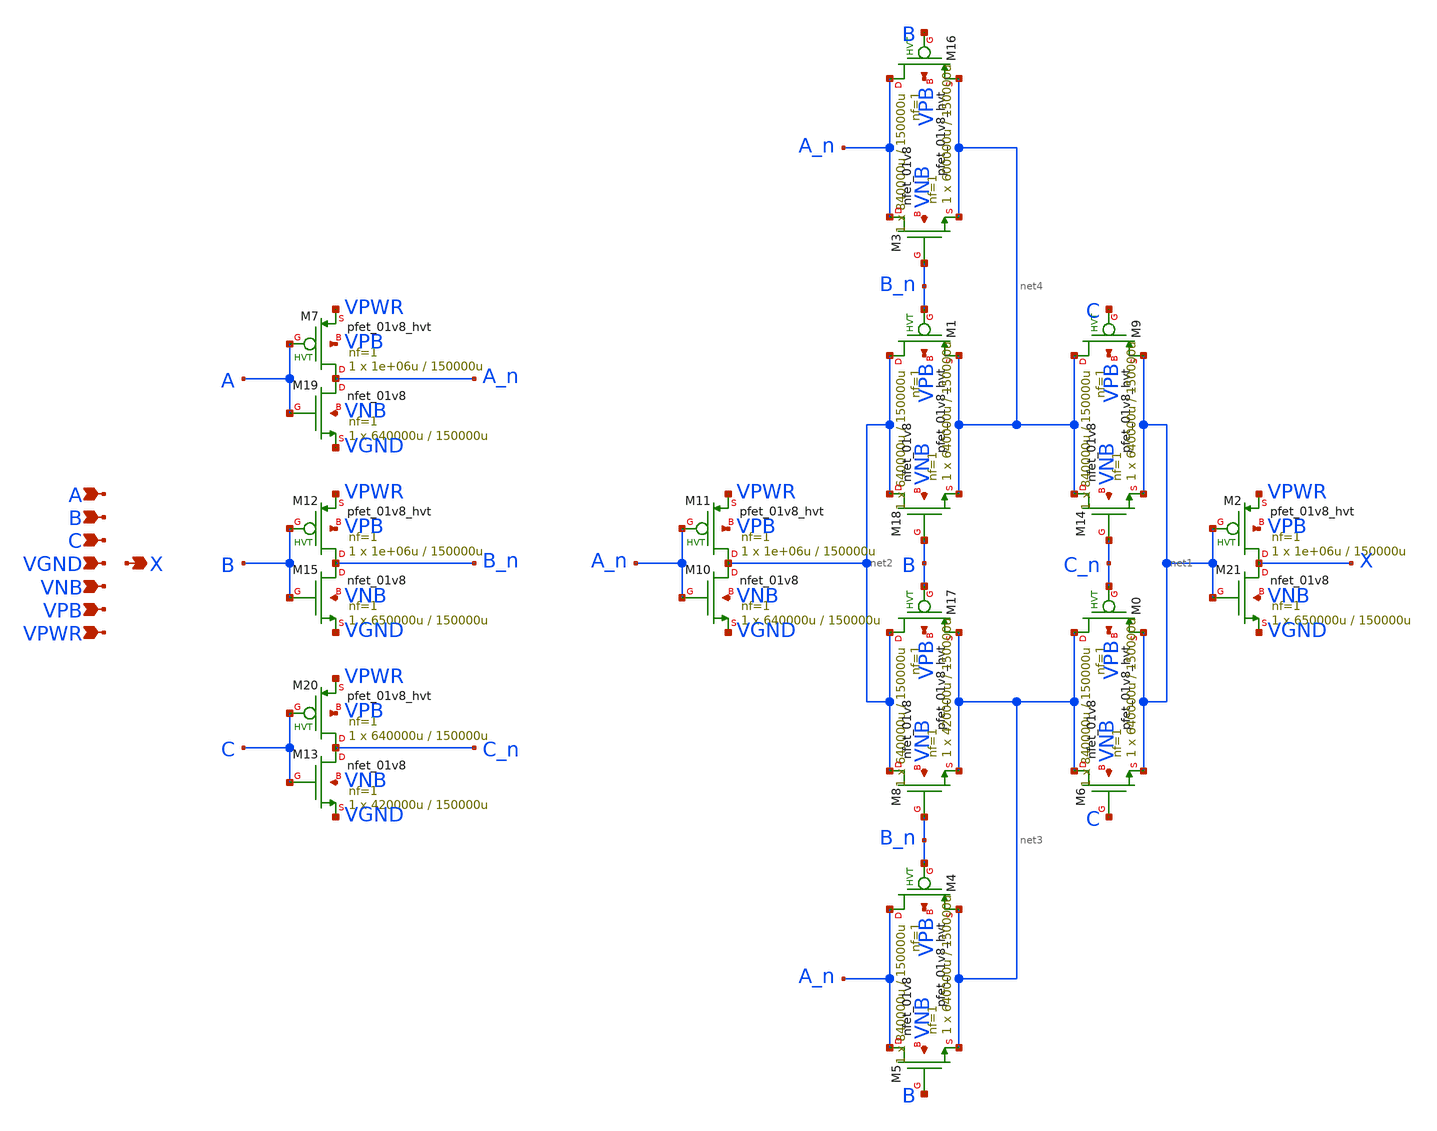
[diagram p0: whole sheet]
** sch_path: schematics/xor3/sky130_fd_sc_hd__xor3_1.sch
**.subckt sky130_fd_sc_hd__xor3_1 A B C VGND VNB VPB VPWR X
*.ipin A
*.ipin B
*.ipin C
*.ipin VGND
*.ipin VNB
*.ipin VPB
*.ipin VPWR
*.opin X
XM7 A_n A VPWR VPB sky130_fd_pr__pfet_01v8_hvt L=150000u W=1e+06u nf=1 ad='int((1 + 1)/2) * 1e+06u / 1 * 0.29'
+ as='int((1 + 2)/2) * 1e+06u / 1 * 0.29' pd='2*int((1 + 1)/2) * (1e+06u / 1 + 0.29)' ps='2*int((1 + 2)/2) * (1e+06u / 1 + 0.29)'
+ nrd='0.29 / 1e+06u ' nrs='0.29 / 1e+06u ' sa=0 sb=0 sd=0 mult=1 m=1
XM19 A_n A VGND VNB sky130_fd_pr__nfet_01v8 L=150000u W=640000u nf=1 ad='int((1 + 1)/2) * 640000u / 1 * 0.29'
+ as='int((1 + 2)/2) * 640000u / 1 * 0.29' pd='2*int((1 + 1)/2) * (640000u / 1 + 0.29)' ps='2*int((1 + 2)/2) * (640000u / 1 + 0.29)'
+ nrd='0.29 / 640000u ' nrs='0.29 / 640000u ' sa=0 sb=0 sd=0 mult=1 m=1
XM2 X net1 VPWR VPB sky130_fd_pr__pfet_01v8_hvt L=150000u W=1e+06u nf=1 ad='int((1 + 1)/2) * 1e+06u / 1 * 0.29'
+ as='int((1 + 2)/2) * 1e+06u / 1 * 0.29' pd='2*int((1 + 1)/2) * (1e+06u / 1 + 0.29)' ps='2*int((1 + 2)/2) * (1e+06u / 1 + 0.29)'
+ nrd='0.29 / 1e+06u ' nrs='0.29 / 1e+06u ' sa=0 sb=0 sd=0 mult=1 m=1
XM21 X net1 VGND VNB sky130_fd_pr__nfet_01v8 L=150000u W=650000u nf=1 ad='int((1 + 1)/2) * 650000u / 1 * 0.29'
+ as='int((1 + 2)/2) * 650000u / 1 * 0.29' pd='2*int((1 + 1)/2) * (650000u / 1 + 0.29)' ps='2*int((1 + 2)/2) * (650000u / 1 + 0.29)'
+ nrd='0.29 / 650000u ' nrs='0.29 / 650000u ' sa=0 sb=0 sd=0 mult=1 m=1
XM11 net2 A_n VPWR VPB sky130_fd_pr__pfet_01v8_hvt L=150000u W=1e+06u nf=1 ad='int((1 + 1)/2) * 1e+06u / 1 * 0.29'
+ as='int((1 + 2)/2) * 1e+06u / 1 * 0.29' pd='2*int((1 + 1)/2) * (1e+06u / 1 + 0.29)' ps='2*int((1 + 2)/2) * (1e+06u / 1 + 0.29)'
+ nrd='0.29 / 1e+06u ' nrs='0.29 / 1e+06u ' sa=0 sb=0 sd=0 mult=1 m=1
XM10 net2 A_n VGND VNB sky130_fd_pr__nfet_01v8 L=150000u W=640000u nf=1 ad='int((1 + 1)/2) * 640000u / 1 * 0.29'
+ as='int((1 + 2)/2) * 640000u / 1 * 0.29' pd='2*int((1 + 1)/2) * (640000u / 1 + 0.29)' ps='2*int((1 + 2)/2) * (640000u / 1 + 0.29)'
+ nrd='0.29 / 640000u ' nrs='0.29 / 640000u ' sa=0 sb=0 sd=0 mult=1 m=1
XM12 B_n B VPWR VPB sky130_fd_pr__pfet_01v8_hvt L=150000u W=1e+06u nf=1 ad='int((1 + 1)/2) * 1e+06u / 1 * 0.29'
+ as='int((1 + 2)/2) * 1e+06u / 1 * 0.29' pd='2*int((1 + 1)/2) * (1e+06u / 1 + 0.29)' ps='2*int((1 + 2)/2) * (1e+06u / 1 + 0.29)'
+ nrd='0.29 / 1e+06u ' nrs='0.29 / 1e+06u ' sa=0 sb=0 sd=0 mult=1 m=1
XM15 B_n B VGND VNB sky130_fd_pr__nfet_01v8 L=150000u W=650000u nf=1 ad='int((1 + 1)/2) * 650000u / 1 * 0.29'
+ as='int((1 + 2)/2) * 650000u / 1 * 0.29' pd='2*int((1 + 1)/2) * (650000u / 1 + 0.29)' ps='2*int((1 + 2)/2) * (650000u / 1 + 0.29)'
+ nrd='0.29 / 650000u ' nrs='0.29 / 650000u ' sa=0 sb=0 sd=0 mult=1 m=1
XM20 C_n C VPWR VPB sky130_fd_pr__pfet_01v8_hvt L=150000u W=640000u nf=1 ad='int((1 + 1)/2) * 640000u / 1 * 0.29'
+ as='int((1 + 2)/2) * 640000u / 1 * 0.29' pd='2*int((1 + 1)/2) * (640000u / 1 + 0.29)' ps='2*int((1 + 2)/2) * (640000u / 1 + 0.29)'
+ nrd='0.29 / 640000u ' nrs='0.29 / 640000u ' sa=0 sb=0 sd=0 mult=1 m=1
XM13 C_n C VGND VNB sky130_fd_pr__nfet_01v8 L=150000u W=420000u nf=1 ad='int((1 + 1)/2) * 420000u / 1 * 0.29'
+ as='int((1 + 2)/2) * 420000u / 1 * 0.29' pd='2*int((1 + 1)/2) * (420000u / 1 + 0.29)' ps='2*int((1 + 2)/2) * (420000u / 1 + 0.29)'
+ nrd='0.29 / 420000u ' nrs='0.29 / 420000u ' sa=0 sb=0 sd=0 mult=1 m=1
XM0 net3 C_n net1 VPB sky130_fd_pr__pfet_01v8_hvt L=150000u W=840000u nf=1 ad='int((1 + 1)/2) * 840000u / 1 * 0.29'
+ as='int((1 + 2)/2) * 840000u / 1 * 0.29' pd='2*int((1 + 1)/2) * (840000u / 1 + 0.29)' ps='2*int((1 + 2)/2) * (840000u / 1 + 0.29)'
+ nrd='0.29 / 840000u ' nrs='0.29 / 840000u ' sa=0 sb=0 sd=0 mult=1 m=1
XM6 net3 C net1 VNB sky130_fd_pr__nfet_01v8 L=150000u W=640000u nf=1 ad='int((1 + 1)/2) * 640000u / 1 * 0.29'
+ as='int((1 + 2)/2) * 640000u / 1 * 0.29' pd='2*int((1 + 1)/2) * (640000u / 1 + 0.29)' ps='2*int((1 + 2)/2) * (640000u / 1 + 0.29)'
+ nrd='0.29 / 640000u ' nrs='0.29 / 640000u ' sa=0 sb=0 sd=0 mult=1 m=1
XM1 net2 B_n net4 VPB sky130_fd_pr__pfet_01v8_hvt L=150000u W=640000u nf=1 ad='int((1 + 1)/2) * 640000u / 1 * 0.29'
+ as='int((1 + 2)/2) * 640000u / 1 * 0.29' pd='2*int((1 + 1)/2) * (640000u / 1 + 0.29)' ps='2*int((1 + 2)/2) * (640000u / 1 + 0.29)'
+ nrd='0.29 / 640000u ' nrs='0.29 / 640000u ' sa=0 sb=0 sd=0 mult=1 m=1
XM18 net2 B net4 VNB sky130_fd_pr__nfet_01v8 L=150000u W=640000u nf=1 ad='int((1 + 1)/2) * 640000u / 1 * 0.29'
+ as='int((1 + 2)/2) * 640000u / 1 * 0.29' pd='2*int((1 + 1)/2) * (640000u / 1 + 0.29)' ps='2*int((1 + 2)/2) * (640000u / 1 + 0.29)'
+ nrd='0.29 / 640000u ' nrs='0.29 / 640000u ' sa=0 sb=0 sd=0 mult=1 m=1
XM4 A_n B_n net3 VPB sky130_fd_pr__pfet_01v8_hvt L=150000u W=840000u nf=1 ad='int((1 + 1)/2) * 840000u / 1 * 0.29'
+ as='int((1 + 2)/2) * 840000u / 1 * 0.29' pd='2*int((1 + 1)/2) * (840000u / 1 + 0.29)' ps='2*int((1 + 2)/2) * (840000u / 1 + 0.29)'
+ nrd='0.29 / 840000u ' nrs='0.29 / 840000u ' sa=0 sb=0 sd=0 mult=1 m=1
XM5 A_n B net3 VNB sky130_fd_pr__nfet_01v8 L=150000u W=640000u nf=1 ad='int((1 + 1)/2) * 640000u / 1 * 0.29'
+ as='int((1 + 2)/2) * 640000u / 1 * 0.29' pd='2*int((1 + 1)/2) * (640000u / 1 + 0.29)' ps='2*int((1 + 2)/2) * (640000u / 1 + 0.29)'
+ nrd='0.29 / 640000u ' nrs='0.29 / 640000u ' sa=0 sb=0 sd=0 mult=1 m=1
XM16 A_n B net4 VPB sky130_fd_pr__pfet_01v8_hvt L=150000u W=840000u nf=1 ad='int((1 + 1)/2) * 840000u / 1 * 0.29'
+ as='int((1 + 2)/2) * 840000u / 1 * 0.29' pd='2*int((1 + 1)/2) * (840000u / 1 + 0.29)' ps='2*int((1 + 2)/2) * (840000u / 1 + 0.29)'
+ nrd='0.29 / 840000u ' nrs='0.29 / 840000u ' sa=0 sb=0 sd=0 mult=1 m=1
XM3 A_n B_n net4 VNB sky130_fd_pr__nfet_01v8 L=150000u W=600000u nf=1 ad='int((1 + 1)/2) * 600000u / 1 * 0.29'
+ as='int((1 + 2)/2) * 600000u / 1 * 0.29' pd='2*int((1 + 1)/2) * (600000u / 1 + 0.29)' ps='2*int((1 + 2)/2) * (600000u / 1 + 0.29)'
+ nrd='0.29 / 600000u ' nrs='0.29 / 600000u ' sa=0 sb=0 sd=0 mult=1 m=1
XM17 net2 B net3 VPB sky130_fd_pr__pfet_01v8_hvt L=150000u W=640000u nf=1 ad='int((1 + 1)/2) * 640000u / 1 * 0.29'
+ as='int((1 + 2)/2) * 640000u / 1 * 0.29' pd='2*int((1 + 1)/2) * (640000u / 1 + 0.29)' ps='2*int((1 + 2)/2) * (640000u / 1 + 0.29)'
+ nrd='0.29 / 640000u ' nrs='0.29 / 640000u ' sa=0 sb=0 sd=0 mult=1 m=1
XM8 net2 B_n net3 VNB sky130_fd_pr__nfet_01v8 L=150000u W=420000u nf=1 ad='int((1 + 1)/2) * 420000u / 1 * 0.29'
+ as='int((1 + 2)/2) * 420000u / 1 * 0.29' pd='2*int((1 + 1)/2) * (420000u / 1 + 0.29)' ps='2*int((1 + 2)/2) * (420000u / 1 + 0.29)'
+ nrd='0.29 / 420000u ' nrs='0.29 / 420000u ' sa=0 sb=0 sd=0 mult=1 m=1
XM9 net4 C net1 VPB sky130_fd_pr__pfet_01v8_hvt L=150000u W=840000u nf=1 ad='int((1 + 1)/2) * 840000u / 1 * 0.29'
+ as='int((1 + 2)/2) * 840000u / 1 * 0.29' pd='2*int((1 + 1)/2) * (840000u / 1 + 0.29)' ps='2*int((1 + 2)/2) * (840000u / 1 + 0.29)'
+ nrd='0.29 / 840000u ' nrs='0.29 / 840000u ' sa=0 sb=0 sd=0 mult=1 m=1
XM14 net4 C_n net1 VNB sky130_fd_pr__nfet_01v8 L=150000u W=640000u nf=1 ad='int((1 + 1)/2) * 640000u / 1 * 0.29'
+ as='int((1 + 2)/2) * 640000u / 1 * 0.29' pd='2*int((1 + 1)/2) * (640000u / 1 + 0.29)' ps='2*int((1 + 2)/2) * (640000u / 1 + 0.29)'
+ nrd='0.29 / 640000u ' nrs='0.29 / 640000u ' sa=0 sb=0 sd=0 mult=1 m=1
**.ends
.end
